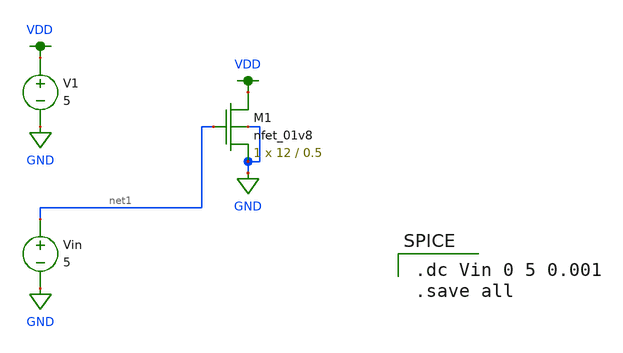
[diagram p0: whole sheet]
** sch_path: mp3/schematics/test_tran.sch
**.subckt test_tran
V1 VDD GND 5
XM1 VDD net1 GND GND sky130_fd_pr__nfet_01v8 L=0.5 W=12 nf=1 ad='int((nf+1)/2) * W/nf * 0.29' as='int((nf+2)/2) * W/nf * 0.29'
+ pd='2*int((nf+1)/2) * (W/nf + 0.29)' ps='2*int((nf+2)/2) * (W/nf + 0.29)' nrd='0.29 / W' nrs='0.29 / W'
+ sa=0 sb=0 sd=0 mult=1 m=1
Vin net1 GND 5
**** begin user architecture code

.option wnflag=1
.lib ~/skywater/skywater-pdk/libraries/sky130_fd_pr_ngspice/latest/models/sky130.lib.spice tt


.dc Vin 0 5 0.001
.save all

**** end user architecture code
**.ends
.GLOBAL GND
.GLOBAL VDD
.end
